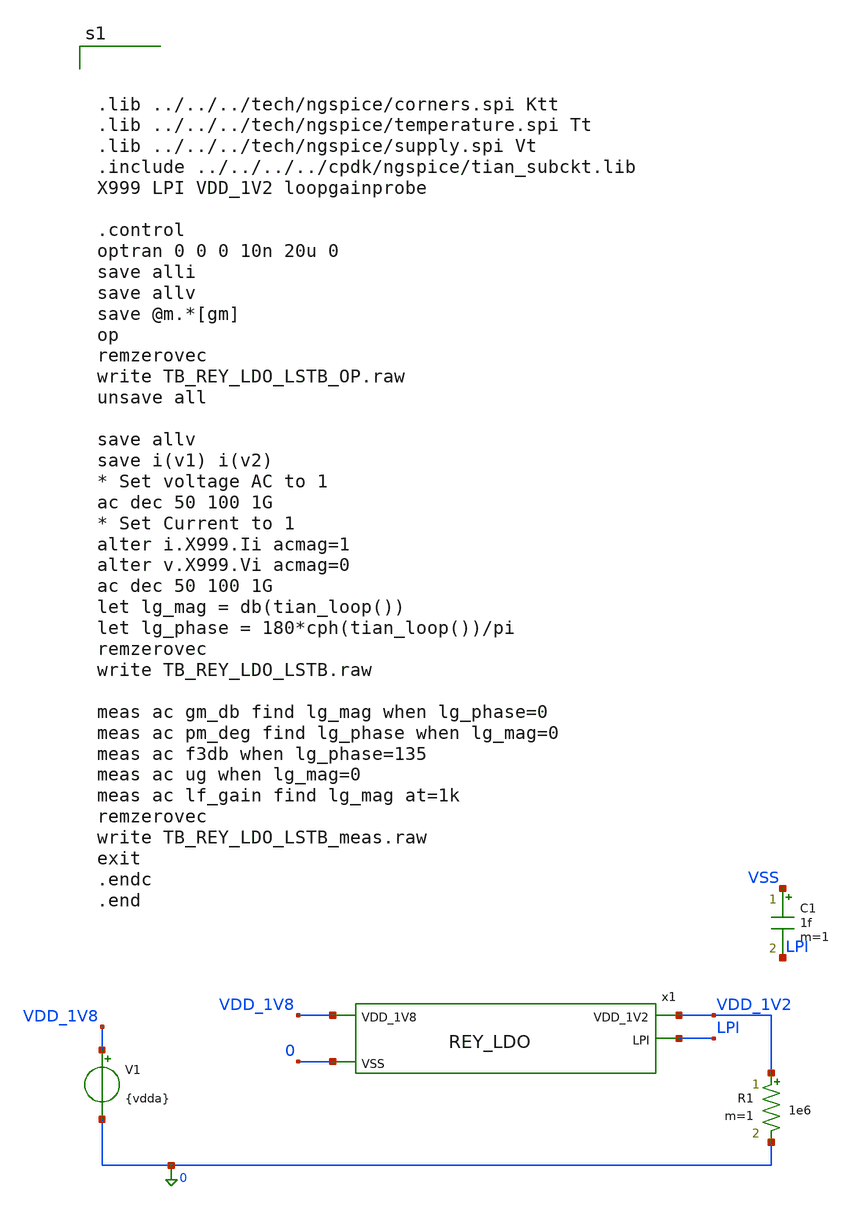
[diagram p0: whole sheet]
** sch_path: design/REY_LDO_SKY130A/TB_REY_LDO_LSTB.sch
**.subckt TB_REY_LDO_LSTB
V1 VDD_1V8 0 {vdda}
C1 VSS LPI 1f m=1
x1 VDD_1V8 VDD_1V2 LPI 0 REY_LDO
R1 VDD_1V2 0 1e6 m=1
**** begin user architecture code



.lib ../../../tech/ngspice/corners.spi Ktt
.lib ../../../tech/ngspice/temperature.spi Tt
.lib ../../../tech/ngspice/supply.spi Vt
.include ../../../../cpdk/ngspice/tian_subckt.lib
X999 LPI VDD_1V2 loopgainprobe

.control
optran 0 0 0 10n 20u 0
save alli
save allv
save @m.*[gm]
op
remzerovec
write TB_REY_LDO_LSTB_OP.raw
unsave all

save allv
save i(v1) i(v2)
* Set voltage AC to 1
ac dec 50 100 1G
* Set Current to 1
alter i.X999.Ii acmag=1
alter v.X999.Vi acmag=0
ac dec 50 100 1G
let lg_mag = db(tian_loop())
let lg_phase = 180*cph(tian_loop())/pi
remzerovec
write TB_REY_LDO_LSTB.raw

meas ac gm_db find lg_mag when lg_phase=0
meas ac pm_deg find lg_phase when lg_mag=0
meas ac f3db when lg_phase=135
meas ac ug when lg_mag=0
meas ac lf_gain find lg_mag at=1k
remzerovec
write TB_REY_LDO_LSTB_meas.raw
exit
.endc
.end



**** end user architecture code
**.ends
.end
